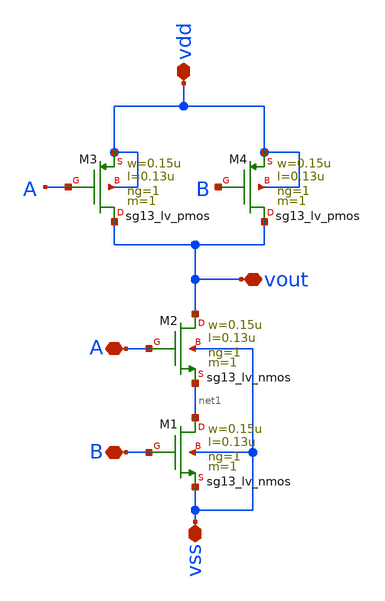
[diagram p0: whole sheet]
** sch_path: design/blocks/puertanand/AND.sch
**.subckt AND vout A B vdd vss
*.iopin vout
*.iopin A
*.iopin B
*.iopin vdd
*.iopin vss
XM1 net1 B vss vss sg13_lv_nmos w=0.15u l=0.13u ng=1 m=1 mm_ok=1
XM2 vout A net1 vss sg13_lv_nmos w=0.15u l=0.13u ng=1 m=1 mm_ok=1
XM3 vout A vdd vdd sg13_lv_pmos w=0.15u l=0.13u ng=1 m=1 mm_ok=1
XM4 vout B vdd vdd sg13_lv_pmos w=0.15u l=0.13u ng=1 m=1 mm_ok=1
**.ends
.end
